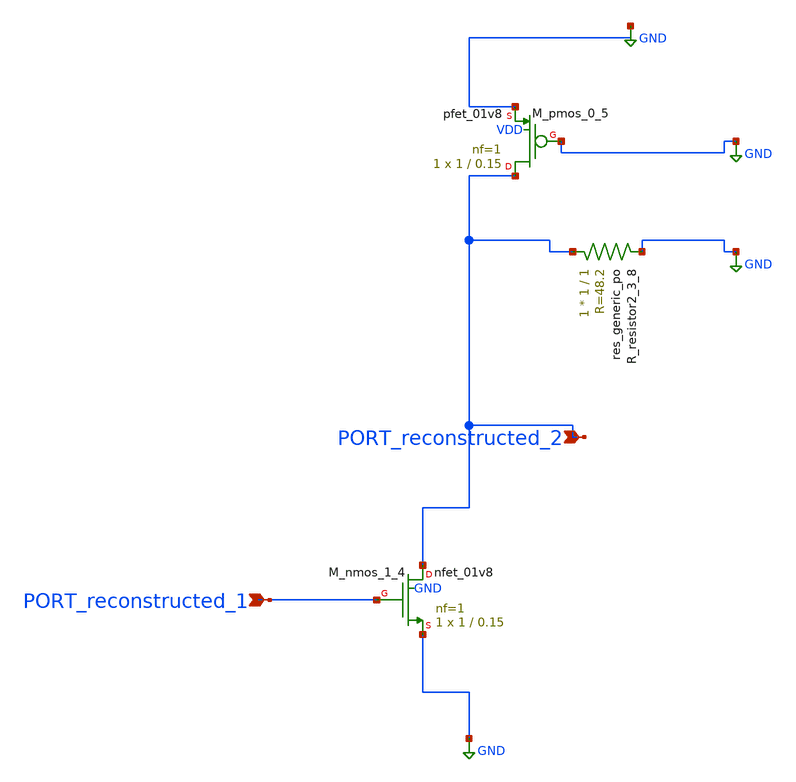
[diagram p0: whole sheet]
** sch_path: schematics/AMSNet/223.sch
**.subckt 223 PORT_reconstructed_1 PORT_reconstructed_2
*.ipin PORT_reconstructed_1
*.ipin PORT_reconstructed_2
XM_nmos_1_4 PORT_reconstructed_2 PORT_reconstructed_1 GND GND sky130_fd_pr__nfet_01v8 L=0.15 W=1 nf=1
+ ad='int((1 + 1)/2) * 1 / 1 * 0.29' as='int((1 + 2)/2) * 1 / 1 * 0.29' pd='2*int((1 + 1)/2) * (1 / 1 + 0.29)'
+ ps='2*int((1 + 2)/2) * (1 / 1 + 0.29)' nrd='0.29 / 1 ' nrs='0.29 / 1 ' sa=0 sb=0 sd=0 mult=1 m=1
XM_pmos_0_5 PORT_reconstructed_2 GND GND VDD sky130_fd_pr__pfet_01v8 L=0.15 W=1 nf=1 ad='int((1 + 1)/2) * 1 / 1 * 0.29'
+ as='int((1 + 2)/2) * 1 / 1 * 0.29' pd='2*int((1 + 1)/2) * (1 / 1 + 0.29)' ps='2*int((1 + 2)/2) * (1 / 1 + 0.29)'
+ nrd='0.29 / 1 ' nrs='0.29 / 1 ' sa=0 sb=0 sd=0 mult=1 m=1
XR_resistor2_3_8 PORT_reconstructed_2 GND sky130_fd_pr__res_generic_po W=1 L=1 m=1
**.ends
.GLOBAL GND
.end
